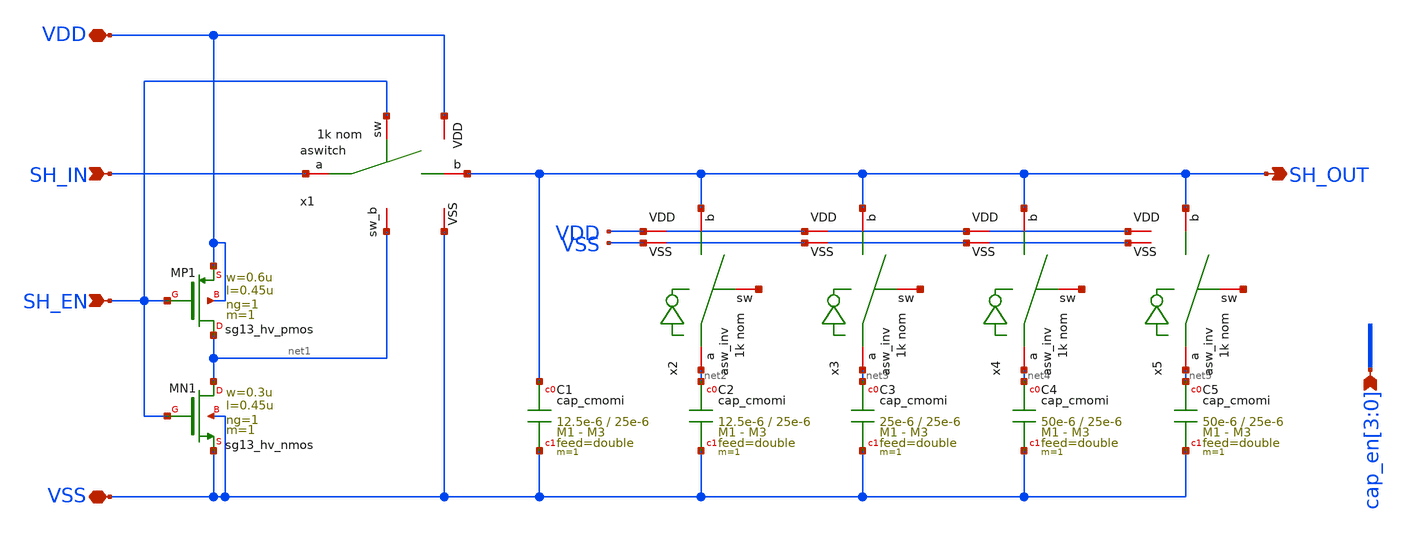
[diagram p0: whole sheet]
** sch_path: macros/heichips26_FAIf/macros/sample_and_hold_trim/schematic/xschem/sample_and_hold_trim.sch
**.subckt sample_and_hold_trim SH_IN SH_EN VDD SH_OUT VSS cap_en[3],cap_en[2],cap_en[1],cap_en[0]
*.ipin SH_IN
*.ipin SH_EN
*.iopin VDD
*.opin SH_OUT
*.iopin VSS
*.ipin cap_en[3],cap_en[2],cap_en[1],cap_en[0]
x1 net1 VDD SH_OUT SH_IN VSS SH_EN aswitch
XC1 SH_OUT VSS cap_cmomi w=12.5e-6 l=25e-6 mmin=1 mmax=3 feed=double subblock=0 m=1 mm_ok=1
XMP1 net1 SH_EN VDD VDD sg13_hv_pmos w=0.6u l=0.45u ng=1 m=1 mm_ok=1
XMN1 net1 SH_EN VSS VSS sg13_hv_nmos w=0.3u l=0.45u ng=1 m=1 mm_ok=1
XC2 net2 VSS cap_cmomi w=12.5e-6 l=25e-6 mmin=1 mmax=3 feed=double subblock=0 m=1 mm_ok=1
XC3 net3 VSS cap_cmomi w=25e-6 l=25e-6 mmin=1 mmax=3 feed=double subblock=0 m=1 mm_ok=1
XC4 net4 VSS cap_cmomi w=50e-6 l=25e-6 mmin=1 mmax=3 feed=double subblock=0 m=1 mm_ok=1
XC5 net5 VSS cap_cmomi w=50e-6 l=25e-6 mmin=1 mmax=3 feed=double subblock=0 m=1 mm_ok=1
x2 VDD SH_OUT net2 VSS net6 asw_inv
x3 VDD SH_OUT net3 VSS net7 asw_inv
x4 VDD SH_OUT net4 VSS net8 asw_inv
x5 VDD SH_OUT net5 VSS net9 asw_inv
**.ends
.end
